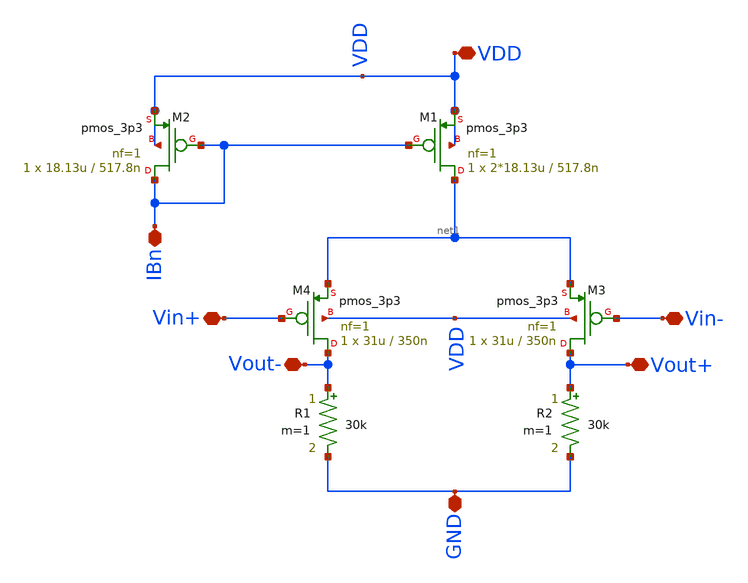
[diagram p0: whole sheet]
** sch_path: ITI_Labs/Lab7/Design/Lab06.sch
**.subckt Lab06 VDD IBn Vin+ Vin- Vout- Vout+ GND
*.iopin VDD
*.iopin IBn
*.iopin Vin+
*.iopin Vin-
*.iopin Vout-
*.iopin Vout+
*.iopin GND
R1 Vout- GND 30k m=1
XM4 Vout- Vin+ net1 VDD pmos_3p3 L=350n W=31u nf=1 ad='int((nf+1)/2) * W/nf * 0.18u' as='int((nf+2)/2) * W/nf * 0.18u'
+ pd='2*int((nf+1)/2) * (W/nf + 0.18u)' ps='2*int((nf+2)/2) * (W/nf + 0.18u)' nrd='0.18u / W' nrs='0.18u / W'
+ sa=0 sb=0 sd=0 m=1
XM1 net1 IBn VDD VDD pmos_3p3 L=517.8n W=2*18.13u nf=1 ad='int((nf+1)/2) * W/nf * 0.18u' as='int((nf+2)/2) * W/nf * 0.18u'
+ pd='2*int((nf+1)/2) * (W/nf + 0.18u)' ps='2*int((nf+2)/2) * (W/nf + 0.18u)' nrd='0.18u / W' nrs='0.18u / W'
+ sa=0 sb=0 sd=0 m=1
XM2 IBn IBn VDD VDD pmos_3p3 L=517.8n W=18.13u nf=1 ad='int((nf+1)/2) * W/nf * 0.18u' as='int((nf+2)/2) * W/nf * 0.18u'
+ pd='2*int((nf+1)/2) * (W/nf + 0.18u)' ps='2*int((nf+2)/2) * (W/nf + 0.18u)' nrd='0.18u / W' nrs='0.18u / W'
+ sa=0 sb=0 sd=0 m=1
XM3 Vout+ Vin- net1 VDD pmos_3p3 L=350n W=31u nf=1 ad='int((nf+1)/2) * W/nf * 0.18u' as='int((nf+2)/2) * W/nf * 0.18u'
+ pd='2*int((nf+1)/2) * (W/nf + 0.18u)' ps='2*int((nf+2)/2) * (W/nf + 0.18u)' nrd='0.18u / W' nrs='0.18u / W'
+ sa=0 sb=0 sd=0 m=1
R2 Vout+ GND 30k m=1
**.ends
.end
